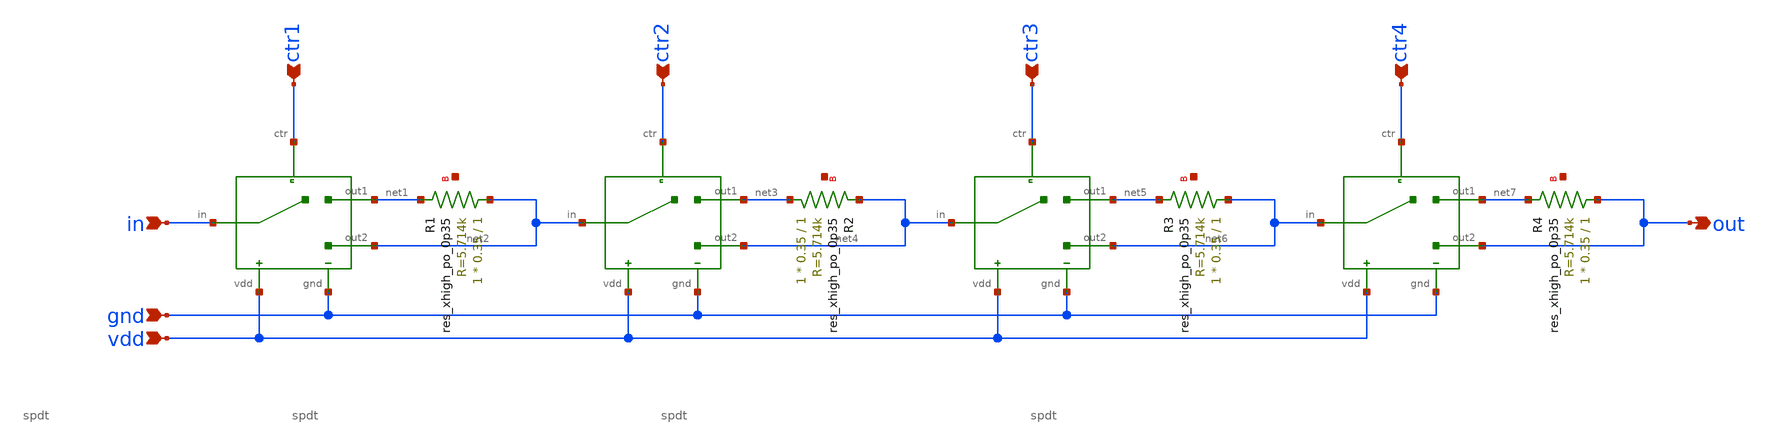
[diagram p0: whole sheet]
** sch_path: xschem/attenuator/dsa.sch
**.subckt dsa in gnd vdd ctr1 ctr2 ctr3 ctr4 out
*.ipin in
*.ipin gnd
*.ipin vdd
*.ipin ctr1
*.ipin ctr2
*.ipin ctr3
*.ipin ctr4
*.opin out
XSPDT1 in ctr1 net1 net2 gnd vdd spdt
XSPDT2 net2 ctr2 net3 net4 gnd vdd spdt
XSPDT3 net4 ctr3 net5 net6 gnd vdd spdt
XSPDT4 net6 ctr4 net7 out gnd vdd spdt
XR1 net2 net1 net8 sky130_fd_pr__res_xhigh_po_0p35 L=1 mult=1 m=1
XR2 net3 net4 net9 sky130_fd_pr__res_xhigh_po_0p35 L=1 mult=1 m=1
XR3 net6 net5 net10 sky130_fd_pr__res_xhigh_po_0p35 L=1 mult=1 m=1
XR4 out net7 net11 sky130_fd_pr__res_xhigh_po_0p35 L=1 mult=1 m=1
**.ends

* expanding   symbol:  /Volumes/WORK_DRIVE/caravel_automatic_gain_control/xschem/attenuator/spdt.sym
*+ # of pins=6
** sym_path: xschem/attenuator/spdt.sym
** sch_path: xschem/attenuator/spdt.sch
.subckt spdt in ctr out1 out2 gnd vdd
*.ipin in
*.ipin ctr
*.ipin gnd
*.ipin vdd
*.opin out1
*.opin out2
XINV1 vdd ctr gnd net1 inverter
XTG1 vdd ctr in gnd net1 out1 transgate
XTG2 vdd net1 in gnd ctr out2 transgate
XINV1 vdd ctr gnd net1 inverter
.ends


* expanding   symbol:
*+  /Volumes/WORK_DRIVE/caravel_automatic_gain_control/xschem/attenuator/inverter.sym # of pins=4
** sym_path: xschem/attenuator/inverter.sym
** sch_path: xschem/attenuator/inverter.sch
.subckt inverter vdd in gnd out
*.ipin in
*.ipin gnd
*.ipin vdd
*.opin out
XM1 out in gnd gnd sky130_fd_pr__nfet_01v8 L=0.15 W=4 nf=1 ad='int((nf+1)/2) * W/nf * 0.29' as='int((nf+2)/2) * W/nf * 0.29'
+ pd='2*int((nf+1)/2) * (W/nf + 0.29)' ps='2*int((nf+2)/2) * (W/nf + 0.29)' nrd='0.29 / W' nrs='0.29 / W'
+ sa=0 sb=0 sd=0 mult=1 m=1
XM2 out in vdd vdd sky130_fd_pr__pfet_01v8 L=0.15 W=4 nf=1 ad='int((nf+1)/2) * W/nf * 0.29' as='int((nf+2)/2) * W/nf * 0.29'
+ pd='2*int((nf+1)/2) * (W/nf + 0.29)' ps='2*int((nf+2)/2) * (W/nf + 0.29)' nrd='0.29 / W' nrs='0.29 / W'
+ sa=0 sb=0 sd=0 mult=1 m=1
.ends


* expanding   symbol:
*+  /Volumes/WORK_DRIVE/caravel_automatic_gain_control/xschem/attenuator/transgate.sym # of pins=6
** sym_path: xschem/attenuator/transgate.sym
** sch_path: xschem/attenuator/transgate.sch
.subckt transgate vdd ctr2 in gnd ctr1 out
*.ipin in
*.ipin ctr2
*.ipin ctr1
*.ipin vdd
*.ipin gnd
*.opin out
XM1 in ctr1 out gnd sky130_fd_pr__nfet_01v8 L=0.15 W=4 nf=1 ad='int((nf+1)/2) * W/nf * 0.29' as='int((nf+2)/2) * W/nf * 0.29'
+ pd='2*int((nf+1)/2) * (W/nf + 0.29)' ps='2*int((nf+2)/2) * (W/nf + 0.29)' nrd='0.29 / W' nrs='0.29 / W'
+ sa=0 sb=0 sd=0 mult=1 m=1
XM2 in ctr2 out vdd sky130_fd_pr__pfet_01v8 L=0.15 W=4 nf=1 ad='int((nf+1)/2) * W/nf * 0.29' as='int((nf+2)/2) * W/nf * 0.29'
+ pd='2*int((nf+1)/2) * (W/nf + 0.29)' ps='2*int((nf+2)/2) * (W/nf + 0.29)' nrd='0.29 / W' nrs='0.29 / W'
+ sa=0 sb=0 sd=0 mult=1 m=1
.ends

.end
